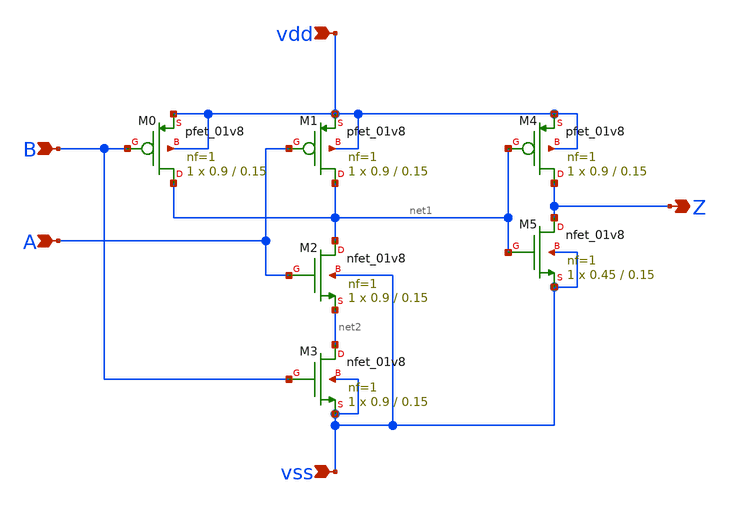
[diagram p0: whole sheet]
** sch_path: track_vlsi/somoza/sch/and.sch
**.subckt and A B vdd Z vss
*.ipin A
*.ipin B
*.ipin vdd
*.opin Z
*.ipin vss
XM2 net1 A net2 vss sky130_fd_pr__nfet_01v8 L=0.15 W=0.9 nf=1 ad='int((nf+1)/2) * W/nf * 0.29' as='int((nf+2)/2) * W/nf * 0.29'
+ pd='2*int((nf+1)/2) * (W/nf + 0.29)' ps='2*int((nf+2)/2) * (W/nf + 0.29)' nrd='0.29 / W' nrs='0.29 / W'
+ sa=0 sb=0 sd=0 mult=1 m=1
XM3 net2 B vss vss sky130_fd_pr__nfet_01v8 L=0.15 W=0.9 nf=1 ad='int((nf+1)/2) * W/nf * 0.29' as='int((nf+2)/2) * W/nf * 0.29'
+ pd='2*int((nf+1)/2) * (W/nf + 0.29)' ps='2*int((nf+2)/2) * (W/nf + 0.29)' nrd='0.29 / W' nrs='0.29 / W'
+ sa=0 sb=0 sd=0 mult=1 m=1
XM1 net1 A vdd vdd sky130_fd_pr__pfet_01v8 L=0.15 W=0.9 nf=1 ad='int((nf+1)/2) * W/nf * 0.29' as='int((nf+2)/2) * W/nf * 0.29'
+ pd='2*int((nf+1)/2) * (W/nf + 0.29)' ps='2*int((nf+2)/2) * (W/nf + 0.29)' nrd='0.29 / W' nrs='0.29 / W'
+ sa=0 sb=0 sd=0 mult=1 m=1
XM0 net1 B vdd vdd sky130_fd_pr__pfet_01v8 L=0.15 W=0.9 nf=1 ad='int((nf+1)/2) * W/nf * 0.29' as='int((nf+2)/2) * W/nf * 0.29'
+ pd='2*int((nf+1)/2) * (W/nf + 0.29)' ps='2*int((nf+2)/2) * (W/nf + 0.29)' nrd='0.29 / W' nrs='0.29 / W'
+ sa=0 sb=0 sd=0 mult=1 m=1
XM4 Z net1 vdd vdd sky130_fd_pr__pfet_01v8 L=0.15 W=0.9 nf=1 ad='int((nf+1)/2) * W/nf * 0.29' as='int((nf+2)/2) * W/nf * 0.29'
+ pd='2*int((nf+1)/2) * (W/nf + 0.29)' ps='2*int((nf+2)/2) * (W/nf + 0.29)' nrd='0.29 / W' nrs='0.29 / W'
+ sa=0 sb=0 sd=0 mult=1 m=1
XM5 Z net1 vss vss sky130_fd_pr__nfet_01v8 L=0.15 W=0.45 nf=1 ad='int((nf+1)/2) * W/nf * 0.29' as='int((nf+2)/2) * W/nf * 0.29'
+ pd='2*int((nf+1)/2) * (W/nf + 0.29)' ps='2*int((nf+2)/2) * (W/nf + 0.29)' nrd='0.29 / W' nrs='0.29 / W'
+ sa=0 sb=0 sd=0 mult=1 m=1
**.ends
.end
